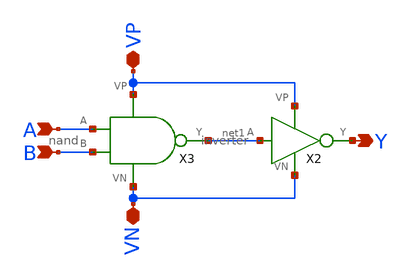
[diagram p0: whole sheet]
** sch_path: schematic/and.sch
**.subckt and A B VP VN Y
*.ipin A
*.ipin B
*.iopin VP
*.iopin VN
*.opin Y
X2 net1 VN VP Y inverter
X3 A B net1 VP VN nand
**.ends

* expanding   symbol:  /home/madvlsi/Documents/neuromorphic_computing_final/schematic/inverter.sym #
*+ of pins=4
** sym_path: schematic/inverter.sym
** sch_path: schematic/inverter.sch
.subckt inverter A VN VP Y
*.ipin A
*.iopin VP
*.iopin VN
*.opin Y
XM1 Y A VN VN sky130_fd_pr__nfet_01v8 L=0.15 W=1 nf=1 ad='int((nf+1)/2) * W/nf * 0.29' as='int((nf+2)/2) * W/nf * 0.29'
+ pd='2*int((nf+1)/2) * (W/nf + 0.29)' ps='2*int((nf+2)/2) * (W/nf + 0.29)' nrd='0.29 / W' nrs='0.29 / W'
+ sa=0 sb=0 sd=0 mult=1 m=1
XM2 Y A VP VP sky130_fd_pr__pfet_01v8 L=0.15 W=1 nf=1 ad='int((nf+1)/2) * W/nf * 0.29' as='int((nf+2)/2) * W/nf * 0.29'
+ pd='2*int((nf+1)/2) * (W/nf + 0.29)' ps='2*int((nf+2)/2) * (W/nf + 0.29)' nrd='0.29 / W' nrs='0.29 / W'
+ sa=0 sb=0 sd=0 mult=1 m=1
.ends


* expanding   symbol:  /home/madvlsi/Documents/neuromorphic_computing_final/schematic/nand.sym # of
*+ pins=5
** sym_path: schematic/nand.sym
** sch_path: schematic/nand.sch
.subckt nand A B Y VP VN
*.ipin A
*.opin Y
*.iopin VP
*.iopin VN
*.ipin B
XM1 Y A VP VP sky130_fd_pr__pfet_01v8 L=0.15 W=1 nf=1 ad='int((nf+1)/2) * W/nf * 0.29' as='int((nf+2)/2) * W/nf * 0.29'
+ pd='2*int((nf+1)/2) * (W/nf + 0.29)' ps='2*int((nf+2)/2) * (W/nf + 0.29)' nrd='0.29 / W' nrs='0.29 / W'
+ sa=0 sb=0 sd=0 mult=1 m=1
XM2 Y B VP VP sky130_fd_pr__pfet_01v8 L=0.15 W=1 nf=1 ad='int((nf+1)/2) * W/nf * 0.29' as='int((nf+2)/2) * W/nf * 0.29'
+ pd='2*int((nf+1)/2) * (W/nf + 0.29)' ps='2*int((nf+2)/2) * (W/nf + 0.29)' nrd='0.29 / W' nrs='0.29 / W'
+ sa=0 sb=0 sd=0 mult=1 m=1
XM3 Y A net1 VN sky130_fd_pr__nfet_01v8 L=0.15 W=1 nf=1 ad='int((nf+1)/2) * W/nf * 0.29' as='int((nf+2)/2) * W/nf * 0.29'
+ pd='2*int((nf+1)/2) * (W/nf + 0.29)' ps='2*int((nf+2)/2) * (W/nf + 0.29)' nrd='0.29 / W' nrs='0.29 / W'
+ sa=0 sb=0 sd=0 mult=1 m=1
XM4 net1 B VN VN sky130_fd_pr__nfet_01v8 L=0.15 W=1 nf=1 ad='int((nf+1)/2) * W/nf * 0.29' as='int((nf+2)/2) * W/nf * 0.29'
+ pd='2*int((nf+1)/2) * (W/nf + 0.29)' ps='2*int((nf+2)/2) * (W/nf + 0.29)' nrd='0.29 / W' nrs='0.29 / W'
+ sa=0 sb=0 sd=0 mult=1 m=1
.ends

.end
